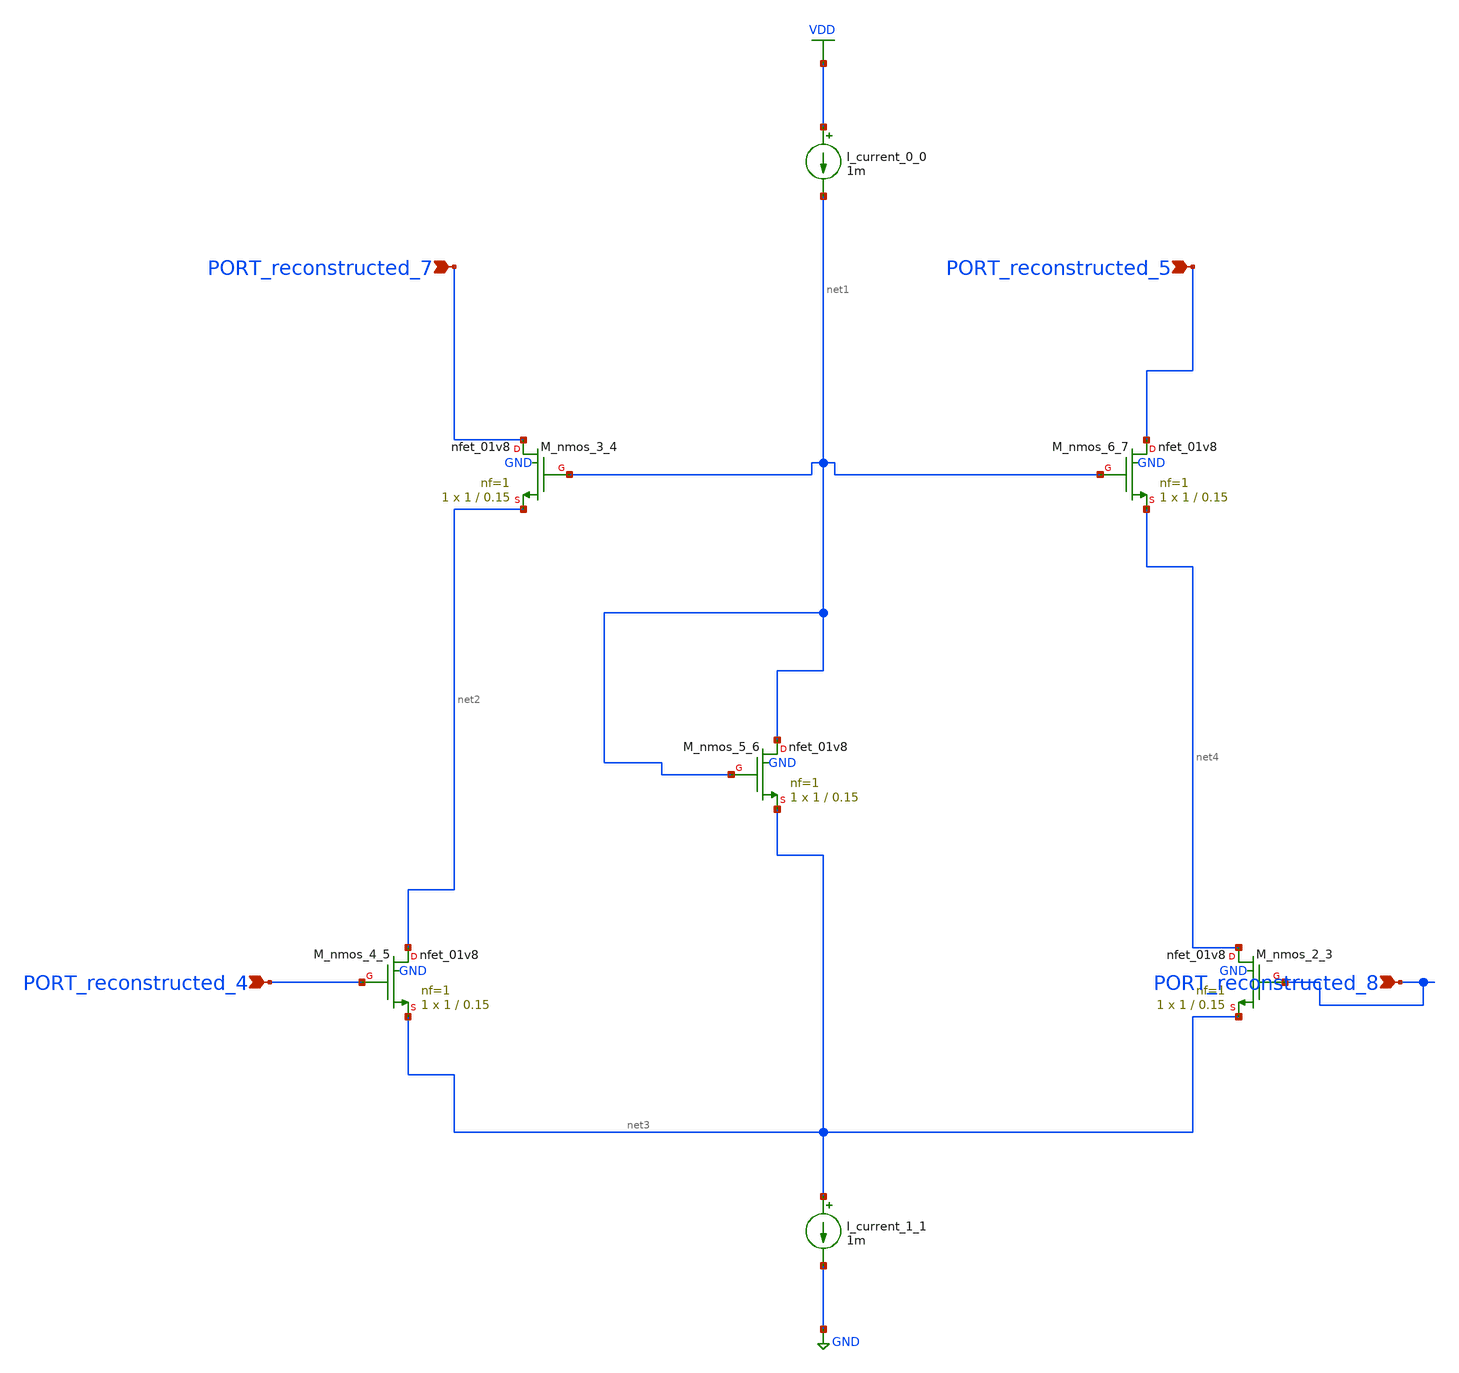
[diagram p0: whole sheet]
** sch_path: schematics/AMSNet/631.sch
**.subckt 631 PORT_reconstructed_7 PORT_reconstructed_8 PORT_reconstructed_4 PORT_reconstructed_5
*.ipin PORT_reconstructed_7
*.ipin PORT_reconstructed_8
*.ipin PORT_reconstructed_4
*.ipin PORT_reconstructed_5
I_current_0_0 VDD net1 1m
I_current_1_1 net3 GND 1m
XM_nmos_2_3 net4 PORT_reconstructed_8 net3 GND sky130_fd_pr__nfet_01v8 L=0.15 W=1 nf=1 ad='int((1 + 1)/2) * 1 / 1 * 0.29'
+ as='int((1 + 2)/2) * 1 / 1 * 0.29' pd='2*int((1 + 1)/2) * (1 / 1 + 0.29)' ps='2*int((1 + 2)/2) * (1 / 1 + 0.29)'
+ nrd='0.29 / 1 ' nrs='0.29 / 1 ' sa=0 sb=0 sd=0 mult=1 m=1
XM_nmos_3_4 PORT_reconstructed_7 net1 net2 GND sky130_fd_pr__nfet_01v8 L=0.15 W=1 nf=1 ad='int((1 + 1)/2) * 1 / 1 * 0.29'
+ as='int((1 + 2)/2) * 1 / 1 * 0.29' pd='2*int((1 + 1)/2) * (1 / 1 + 0.29)' ps='2*int((1 + 2)/2) * (1 / 1 + 0.29)'
+ nrd='0.29 / 1 ' nrs='0.29 / 1 ' sa=0 sb=0 sd=0 mult=1 m=1
XM_nmos_4_5 net2 PORT_reconstructed_4 net3 GND sky130_fd_pr__nfet_01v8 L=0.15 W=1 nf=1 ad='int((1 + 1)/2) * 1 / 1 * 0.29'
+ as='int((1 + 2)/2) * 1 / 1 * 0.29' pd='2*int((1 + 1)/2) * (1 / 1 + 0.29)' ps='2*int((1 + 2)/2) * (1 / 1 + 0.29)'
+ nrd='0.29 / 1 ' nrs='0.29 / 1 ' sa=0 sb=0 sd=0 mult=1 m=1
XM_nmos_5_6 net1 net1 net3 GND sky130_fd_pr__nfet_01v8 L=0.15 W=1 nf=1 ad='int((1 + 1)/2) * 1 / 1 * 0.29'
+ as='int((1 + 2)/2) * 1 / 1 * 0.29' pd='2*int((1 + 1)/2) * (1 / 1 + 0.29)' ps='2*int((1 + 2)/2) * (1 / 1 + 0.29)'
+ nrd='0.29 / 1 ' nrs='0.29 / 1 ' sa=0 sb=0 sd=0 mult=1 m=1
XM_nmos_6_7 PORT_reconstructed_5 net1 net4 GND sky130_fd_pr__nfet_01v8 L=0.15 W=1 nf=1 ad='int((1 + 1)/2) * 1 / 1 * 0.29'
+ as='int((1 + 2)/2) * 1 / 1 * 0.29' pd='2*int((1 + 1)/2) * (1 / 1 + 0.29)' ps='2*int((1 + 2)/2) * (1 / 1 + 0.29)'
+ nrd='0.29 / 1 ' nrs='0.29 / 1 ' sa=0 sb=0 sd=0 mult=1 m=1
**.ends
.GLOBAL GND
.GLOBAL VDD
.end
